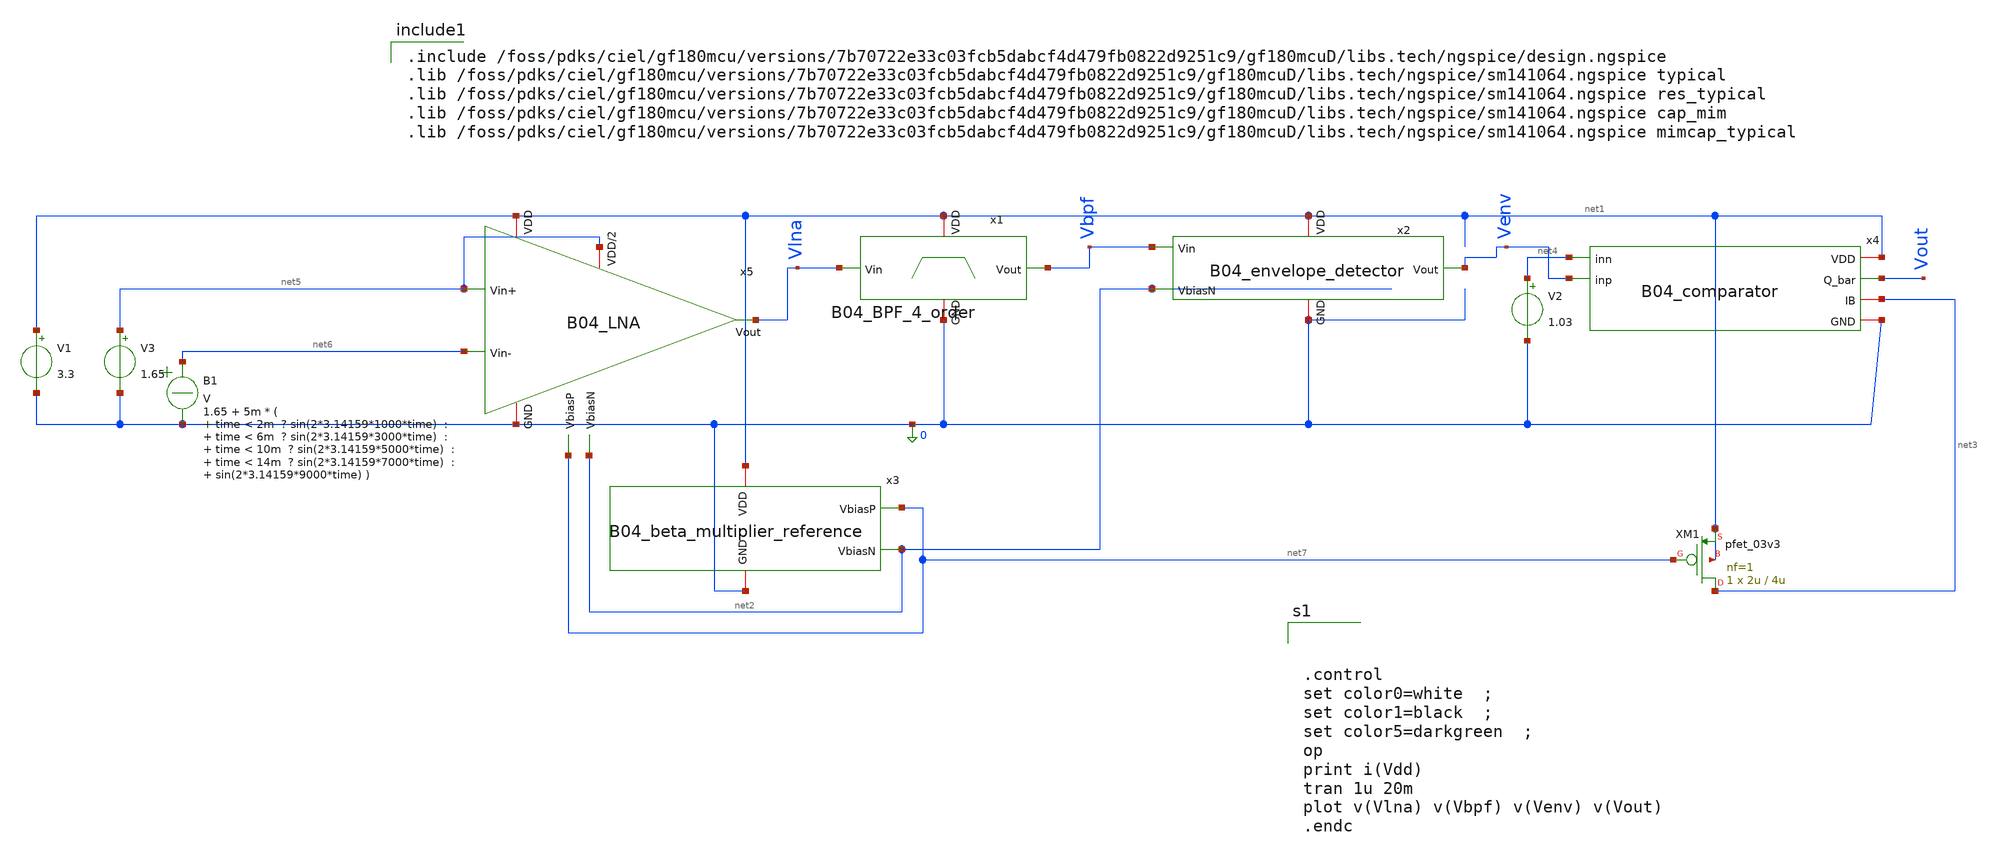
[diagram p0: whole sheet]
** sch_path: analog/B04_tb_AFE.sch
**.subckt B04_tb_AFE
x1 net1 Vbpf Vlna 0 B04_BPF_4_order
V1 net1 0 3.3
B1 net6 0 V = 1.65 + 5m * ( time < 2m ? sin(2*3.14159*1000*time) : time < 6m ?
+ sin(2*3.14159*3000*time) : time < 10m ? sin(2*3.14159*5000*time) : time < 14m ? sin(2*3.14159*7000*time) :
+ sin(2*3.14159*9000*time) )
x2 net1 Vbpf Venv 0 net2 B04_envelope_detector
x3 net1 net7 net2 0 B04_beta_multiplier_reference length=410u
x4 net1 Vout net4 Venv net3 0 B04_comparator
V2 net4 0 1.03
x5 net1 net5 net5 Vlna net6 0 net7 net2 B04_LNA
V3 net5 0 1.65
XM1 net3 net7 net1 net1 pfet_03v3 L=4u W=2u nf=1 ad='int((nf+1)/2) * W/nf * 0.18u' as='int((nf+2)/2) * W/nf * 0.18u'
+ pd='2*int((nf+1)/2) * (W/nf + 0.18u)' ps='2*int((nf+2)/2) * (W/nf + 0.18u)' nrd='0.18u / W' nrs='0.18u / W'
+ sa=0 sb=0 sd=0 m=1
**** begin user architecture code

.include /foss/pdks/ciel/gf180mcu/versions/7b70722e33c03fcb5dabcf4d479fb0822d9251c9/gf180mcuD/libs.tech/ngspice/design.ngspice
.lib /foss/pdks/ciel/gf180mcu/versions/7b70722e33c03fcb5dabcf4d479fb0822d9251c9/gf180mcuD/libs.tech/ngspice/sm141064.ngspice typical
.lib /foss/pdks/ciel/gf180mcu/versions/7b70722e33c03fcb5dabcf4d479fb0822d9251c9/gf180mcuD/libs.tech/ngspice/sm141064.ngspice res_typical
.lib /foss/pdks/ciel/gf180mcu/versions/7b70722e33c03fcb5dabcf4d479fb0822d9251c9/gf180mcuD/libs.tech/ngspice/sm141064.ngspice cap_mim
.lib /foss/pdks/ciel/gf180mcu/versions/7b70722e33c03fcb5dabcf4d479fb0822d9251c9/gf180mcuD/libs.tech/ngspice/sm141064.ngspice mimcap_typical




.control
set color0=white  ;
set color1=black  ;
set color5=darkgreen  ;
op
print i(Vdd)
tran 1u 20m
plot v(Vlna) v(Vbpf) v(Venv) v(Vout)
.endc


**** end user architecture code
**.ends
.end
